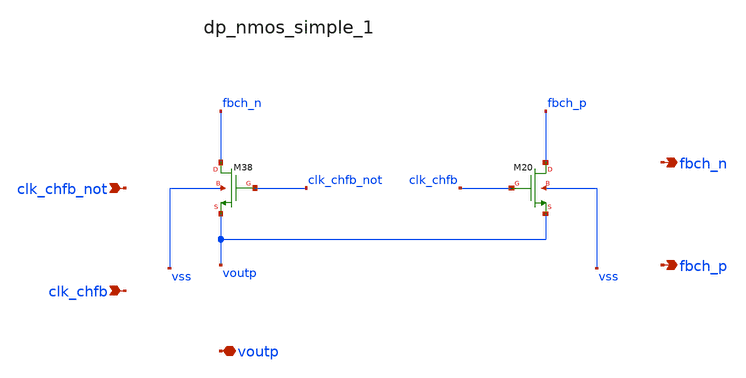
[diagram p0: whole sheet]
** sch_path: analog-db/raw/ia_002_fan_chopper_simple/hier/blocks/dp_nmos_simple_1.sch
**.subckt dp_nmos_simple_1 clk_chfb_not clk_chfb voutp fbch_n fbch_p
*.ipin clk_chfb_not
*.ipin clk_chfb
*.iopin voutp
*.opin fbch_n
*.opin fbch_p
XM20 fbch_p clk_chfb voutp vss sg13_lv_nmos w=x_dut_xm20_w l=x_dut_xm20_l ng=1 m=x_dut_xm20_m
XM38 fbch_n clk_chfb_not voutp vss sg13_lv_nmos w=x_dut_xm38_w l=x_dut_xm38_l ng=1 m=x_dut_xm38_m
**.ends
.end
